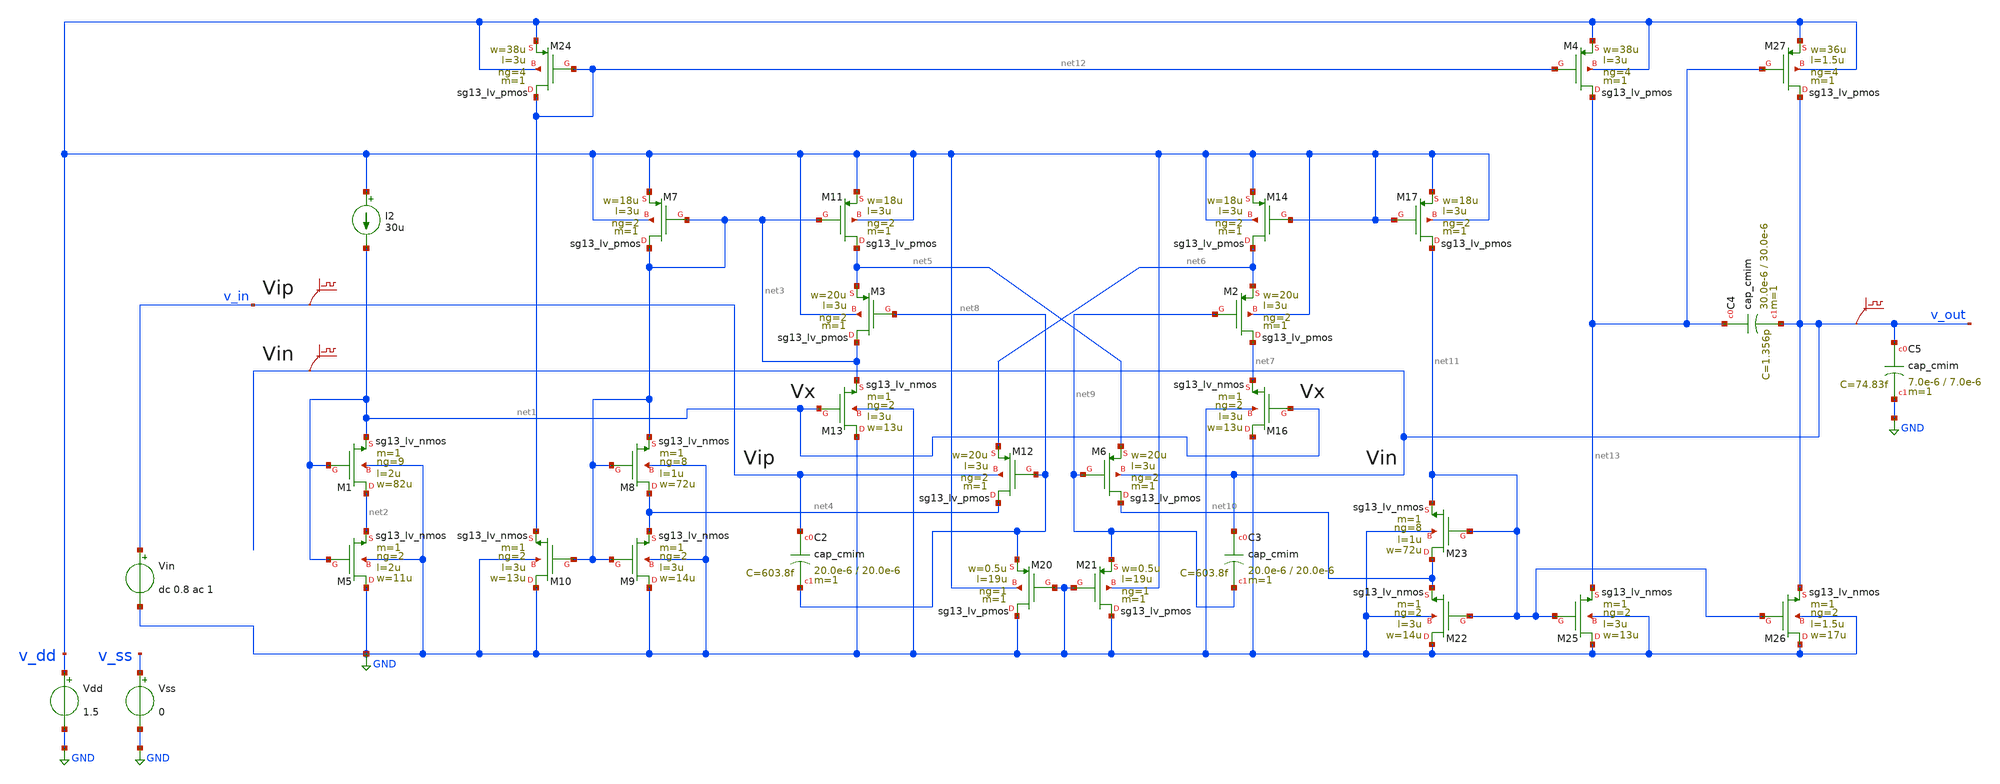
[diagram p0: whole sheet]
** sch_path: 3_Real_Cir/10_Real_Cir/test_Real_Cir/Improved/improved_5t_bulk-driven_ota_A.sch
* Copyright 2023 IHP PDK Authors
* Licensed under the Apache License, Version 2.0 (the "License");
* you may not use this file except in compliance with the License.
* You may obtain a copy of the License at
* https://www.apache.org/licenses/LICENSE-2.0
* Unless required by applicable law or agreed to in writing, software
* distributed under the License is distributed on an "AS IS" BASIS,
* WITHOUT WARRANTIES OR CONDITIONS OF ANY KIND, either express or implied.
* See the License for the specific language governing permissions and
* limitations under the License.
* Copyright 2024 IHP PDK Authors
**.subckt improved_5t_bulk-driven_ota_A
Vdd v_dd GND 1.5
Vss v_ss GND 0
XM4 net13 net12 v_dd v_dd sg13_lv_pmos w=38u l=3u ng=4 m=1 mm_ok=1
I2 v_dd net1 30u
XM1 net2 net1 net1 GND sg13_lv_nmos w=82u l=2u ng=9 m=1 mm_ok=1
XM5 GND net1 net2 GND sg13_lv_nmos w=11u l=2u ng=2 m=1 mm_ok=1
XM7 net3 net3 v_dd v_dd sg13_lv_pmos w=18u l=3u ng=2 m=1 mm_ok=1
XM8 net4 net3 net3 GND sg13_lv_nmos w=72u l=1u ng=8 m=1 mm_ok=1
XM9 GND net3 net4 GND sg13_lv_nmos w=14u l=3u ng=2 m=1 mm_ok=1
XM10 GND net3 net12 GND sg13_lv_nmos w=13u l=3u ng=2 m=1 mm_ok=1
XM11 net5 net3 v_dd v_dd sg13_lv_pmos w=18u l=3u ng=2 m=1 mm_ok=1
XM13 GND net1 net3 GND sg13_lv_nmos w=13u l=3u ng=2 m=1 mm_ok=1
XM14 net6 v_dd v_dd v_dd sg13_lv_pmos w=18u l=3u ng=2 m=1 mm_ok=1
XM16 GND net1 net7 GND sg13_lv_nmos w=13u l=3u ng=2 m=1 mm_ok=1
XM17 net11 v_dd v_dd v_dd sg13_lv_pmos w=18u l=3u ng=2 m=1 mm_ok=1
XM20 GND GND net8 v_dd sg13_lv_pmos w=0.5u l=19u ng=1 m=1 mm_ok=1
XM21 GND GND net9 v_dd sg13_lv_pmos w=0.5u l=19u ng=1 m=1 mm_ok=1
XC2 v_in net8 cap_cmim w=20.0e-6 l=20.0e-6 m=1 mm_ok=1
XC3 v_out net9 cap_cmim w=20.0e-6 l=20.0e-6 m=1 mm_ok=1
XM22 GND net11 net10 GND sg13_lv_nmos w=14u l=3u ng=2 m=1 mm_ok=1
XM23 net10 net11 net11 GND sg13_lv_nmos w=72u l=1u ng=8 m=1 mm_ok=1
XM24 net12 net12 v_dd v_dd sg13_lv_pmos w=38u l=3u ng=4 m=1 mm_ok=1
XM25 GND net11 net13 GND sg13_lv_nmos w=13u l=3u ng=2 m=1 mm_ok=1
XM26 GND net11 v_out GND sg13_lv_nmos w=17u l=1.5u ng=2 m=1 mm_ok=1
XM27 v_out net13 v_dd v_dd sg13_lv_pmos w=36u l=1.5u ng=4 m=1 mm_ok=1
XC4 net13 v_out cap_cmim w=30.0e-6 l=30.0e-6 m=1 mm_ok=1
XC5 v_out GND cap_cmim w=7.0e-6 l=7.0e-6 m=1 mm_ok=1
.save v(v_in)
.save v(v_out)
.save v(v_out)
XM2 net7 net9 net6 v_dd sg13_lv_pmos w=20u l=3u ng=2 m=1 mm_ok=1
XM3 net3 net8 net5 v_dd sg13_lv_pmos w=20u l=3u ng=2 m=1 mm_ok=1
Vin v_in GND dc 0.8 ac 1
XM6 net10 net9 net5 v_out sg13_lv_pmos w=20u l=3u ng=2 m=1 mm_ok=1
XM12 net4 net8 net6 v_in sg13_lv_pmos w=20u l=3u ng=2 m=1 mm_ok=1
**** begin user architecture code


.temp 27
.control
option sparse
save all

*tran 10n 10u
*write eaa_improved_5t_bulk-driven_ota.raw
*plot v(v_inp) v(v_inn) v(v_out)

.title Bulk Driven OTA

op
write ota-improved_tb-ac.raw
set appendwrite

ac dec 101 1k 1G
write eaa_improved_5t_bulk-driven_ota.raw
plot 20*log10(v_out)

meas ac dcgain MAX vmag(v_out) FROM=10 TO=10k
let f3db = dcgain/sqrt(2)
meas ac fbw WHEN vmag(v_out)=f3db FALL=1
let gainerror=(dcgain-1)/1
print dcgain
print fbw
print gainerror

noise v(v_out) Vin dec 101 1k 100MEG 1000
print onoise_total

.endc


 .lib $::SG13G2_MODELS/cornerMOSlv.lib mos_tt
.lib $::SG13G2_MODELS/cornerCAP.lib cap_typ
.lib $::SG13G2_MODELS/cornerRES.lib res_typ
.inc $::PDK_ROOT/ihp-sg13g2/libs.ref/sg13g2_stdcell/spice/sg13g2_stdcell.spice

**** end user architecture code
**.ends
.GLOBAL GND
.end
